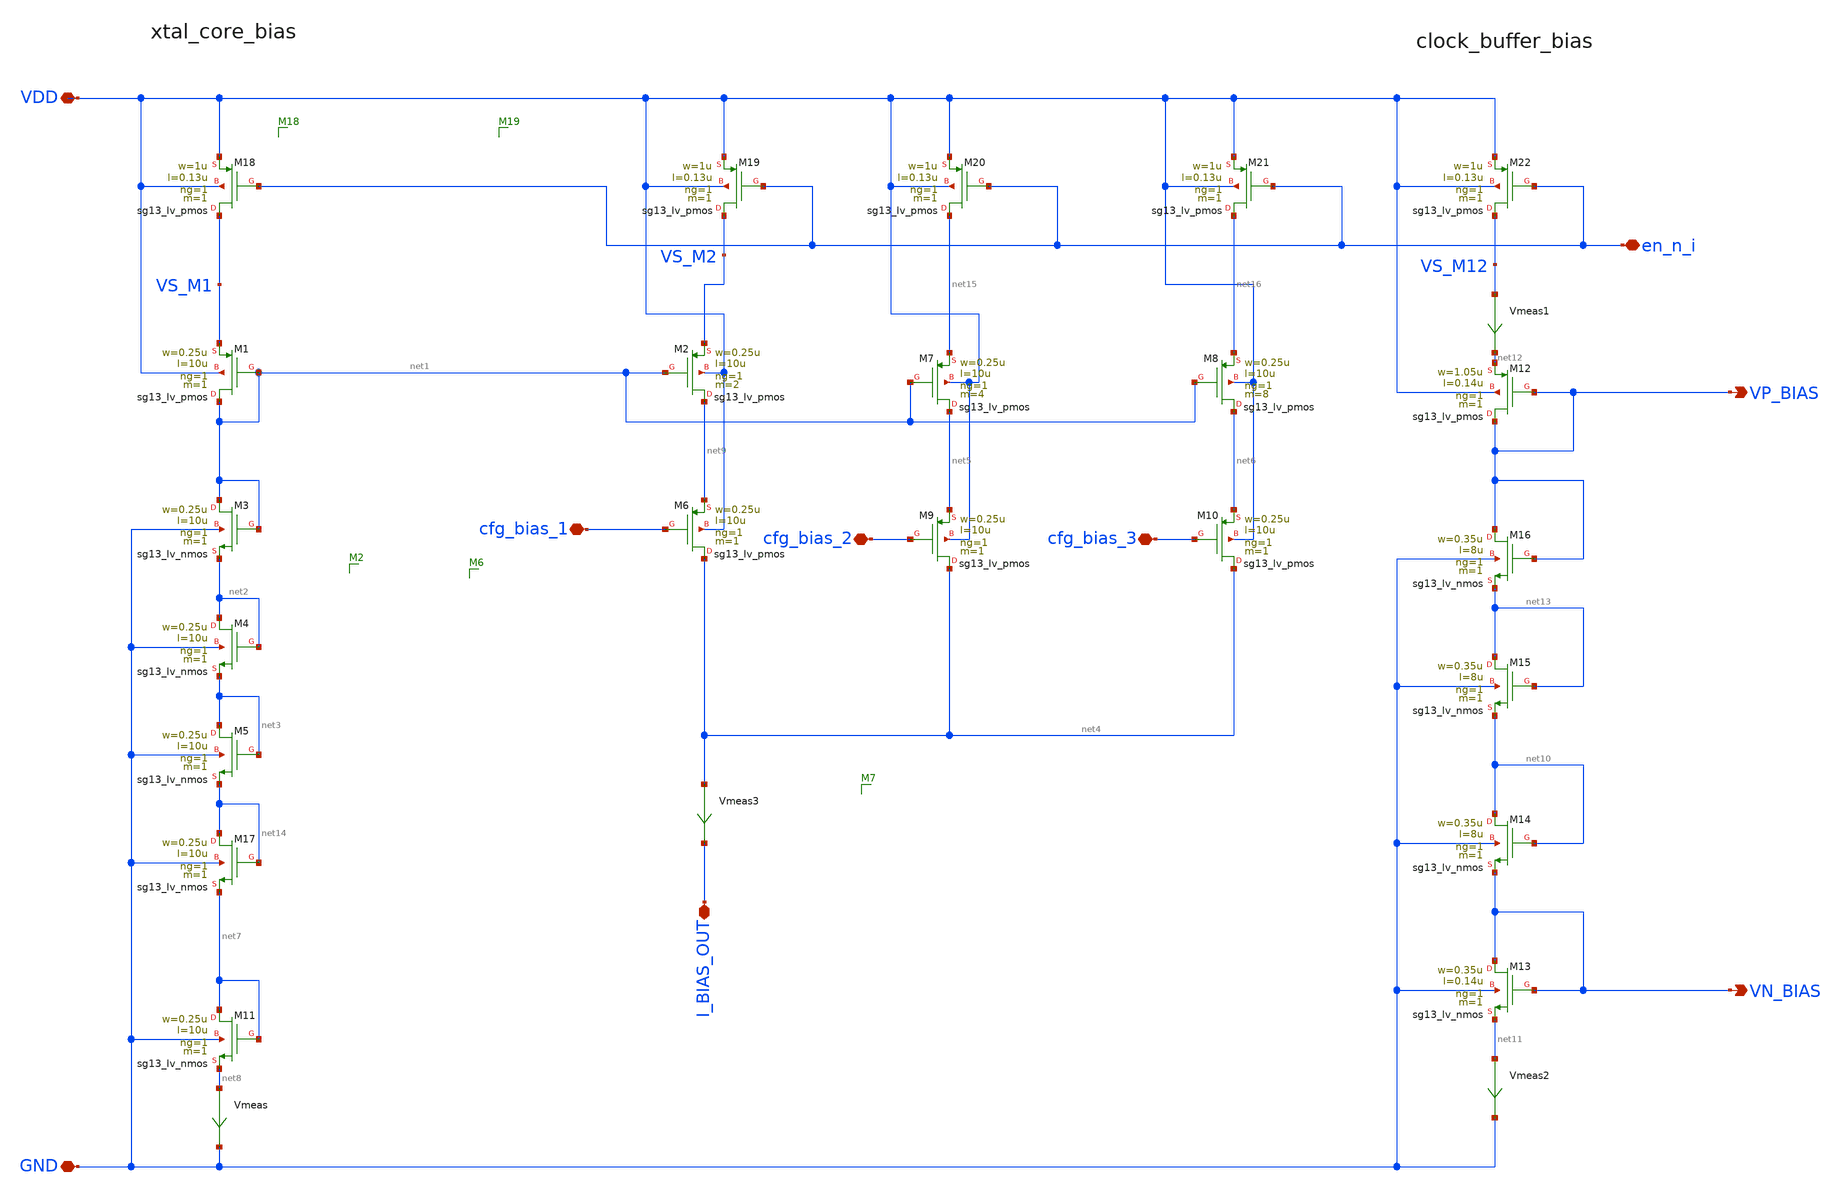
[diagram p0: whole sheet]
** sch_path: osc_bias.sch
**.subckt osc_bias VDD GND I_BIAS_OUT cfg_bias_1 cfg_bias_2 cfg_bias_3 VN_BIAS VP_BIAS en_n_i
*.iopin VDD
*.iopin GND
*.iopin I_BIAS_OUT
*.iopin cfg_bias_1
*.iopin cfg_bias_2
*.iopin cfg_bias_3
*.opin VN_BIAS
*.opin VP_BIAS
*.iopin en_n_i
XM1 net1 net1 VS_M1 VDD sg13_lv_pmos w=0.25u l=10u ng=1 m=1 mm_ok=1
XM3 net1 net1 net2 GND sg13_lv_nmos w=0.25u l=10u ng=1 m=1 mm_ok=1
XM4 net2 net2 net3 GND sg13_lv_nmos w=0.25u l=10u ng=1 m=1 mm_ok=1
XM5 net3 net3 net14 GND sg13_lv_nmos w=0.25u l=10u ng=1 m=1 mm_ok=1
XM2 net9 net1 VS_M2 VDD sg13_lv_pmos w=0.25u l=10u ng=1 m=2 mm_ok=1
XM6 net4 cfg_bias_1 net9 VDD sg13_lv_pmos w=0.25u l=10u ng=1 m=1 mm_ok=1
XM7 net5 net1 net15 VDD sg13_lv_pmos w=0.25u l=10u ng=1 m=4 mm_ok=1
XM8 net6 net1 net16 VDD sg13_lv_pmos w=0.25u l=10u ng=1 m=8 mm_ok=1
XM9 net4 cfg_bias_2 net5 VDD sg13_lv_pmos w=0.25u l=10u ng=1 m=1 mm_ok=1
XM10 net4 cfg_bias_3 net6 VDD sg13_lv_pmos w=0.25u l=10u ng=1 m=1 mm_ok=1
XM11 net7 net7 net8 GND sg13_lv_nmos w=0.25u l=10u ng=1 m=1 mm_ok=1
Vmeas net8 GND 0
.save i(vmeas)
XM12 VP_BIAS VP_BIAS net12 VDD sg13_lv_pmos w=1.05u l=0.14u ng=1 m=1 mm_ok=1
XM13 VN_BIAS VN_BIAS net11 GND sg13_lv_nmos w=0.35u l=0.14u ng=1 m=1 mm_ok=1
Vmeas1 VS_M12 net12 0
.save i(vmeas1)
Vmeas2 net11 GND 0
.save i(vmeas2)
XM14 net10 net10 VN_BIAS GND sg13_lv_nmos w=0.35u l=8u ng=1 m=1 mm_ok=1
XM15 net13 net13 net10 GND sg13_lv_nmos w=0.35u l=8u ng=1 m=1 mm_ok=1
XM16 VP_BIAS VP_BIAS net13 GND sg13_lv_nmos w=0.35u l=8u ng=1 m=1 mm_ok=1
XM17 net14 net14 net7 GND sg13_lv_nmos w=0.25u l=10u ng=1 m=1 mm_ok=1
Vmeas3 net4 I_BIAS_OUT 0
.save i(vmeas3)
XM18 VS_M1 en_n_i VDD VDD sg13_lv_pmos w=1u l=0.13u ng=1 m=1 mm_ok=1
XM19 VS_M2 en_n_i VDD VDD sg13_lv_pmos w=1u l=0.13u ng=1 m=1 mm_ok=1
XM20 net15 en_n_i VDD VDD sg13_lv_pmos w=1u l=0.13u ng=1 m=1 mm_ok=1
XM21 net16 en_n_i VDD VDD sg13_lv_pmos w=1u l=0.13u ng=1 m=1 mm_ok=1
XM22 VS_M12 en_n_i VDD VDD sg13_lv_pmos w=1u l=0.13u ng=1 m=1 mm_ok=1
**.ends
.end
